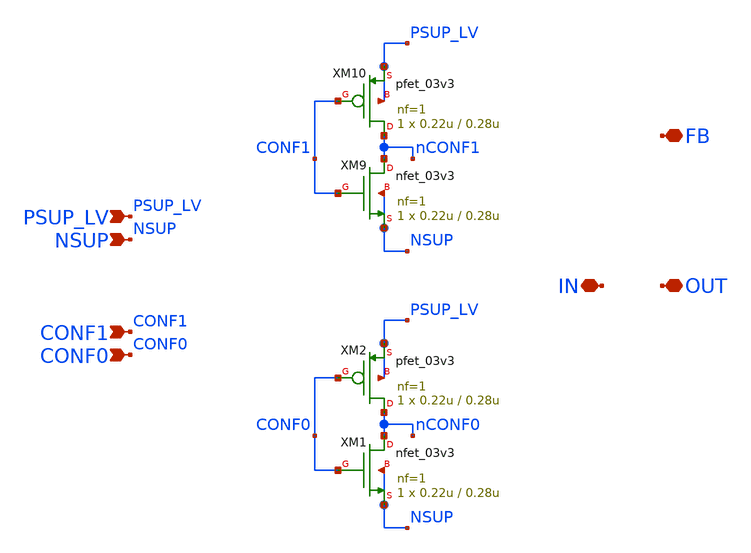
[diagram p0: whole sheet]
** sch_path: xschem/blocks/LPF_freq_fb/LPF_freq_fb.sch
**.subckt LPF_freq_fb PSUP_LV NSUP CONF1 CONF0 IN OUT FB
*.ipin PSUP_LV
*.ipin NSUP
*.ipin CONF1
*.ipin CONF0
*.iopin IN
*.iopin OUT
*.iopin FB
XM9 nCONF1 CONF1 NSUP NSUP nfet_03v3 L=0.28u W=0.22u nf=1 ad='int((nf+1)/2) * W/nf * 0.18u' as='int((nf+2)/2) * W/nf * 0.18u'
+ pd='2*int((nf+1)/2) * (W/nf + 0.18u)' ps='2*int((nf+2)/2) * (W/nf + 0.18u)' nrd='0.18u / W' nrs='0.18u / W'
+ sa=0 sb=0 sd=0 m=1
XM10 nCONF1 CONF1 PSUP_LV PSUP_LV pfet_03v3 L=0.28u W=0.22u nf=1 ad='int((nf+1)/2) * W/nf * 0.18u' as='int((nf+2)/2) * W/nf * 0.18u'
+ pd='2*int((nf+1)/2) * (W/nf + 0.18u)' ps='2*int((nf+2)/2) * (W/nf + 0.18u)' nrd='0.18u / W' nrs='0.18u / W'
+ sa=0 sb=0 sd=0 m=1
XM1 nCONF0 CONF0 NSUP NSUP nfet_03v3 L=0.28u W=0.22u nf=1 ad='int((nf+1)/2) * W/nf * 0.18u' as='int((nf+2)/2) * W/nf * 0.18u'
+ pd='2*int((nf+1)/2) * (W/nf + 0.18u)' ps='2*int((nf+2)/2) * (W/nf + 0.18u)' nrd='0.18u / W' nrs='0.18u / W'
+ sa=0 sb=0 sd=0 m=1
XM2 nCONF0 CONF0 PSUP_LV PSUP_LV pfet_03v3 L=0.28u W=0.22u nf=1 ad='int((nf+1)/2) * W/nf * 0.18u' as='int((nf+2)/2) * W/nf * 0.18u'
+ pd='2*int((nf+1)/2) * (W/nf + 0.18u)' ps='2*int((nf+2)/2) * (W/nf + 0.18u)' nrd='0.18u / W' nrs='0.18u / W'
+ sa=0 sb=0 sd=0 m=1
**.ends
.end
